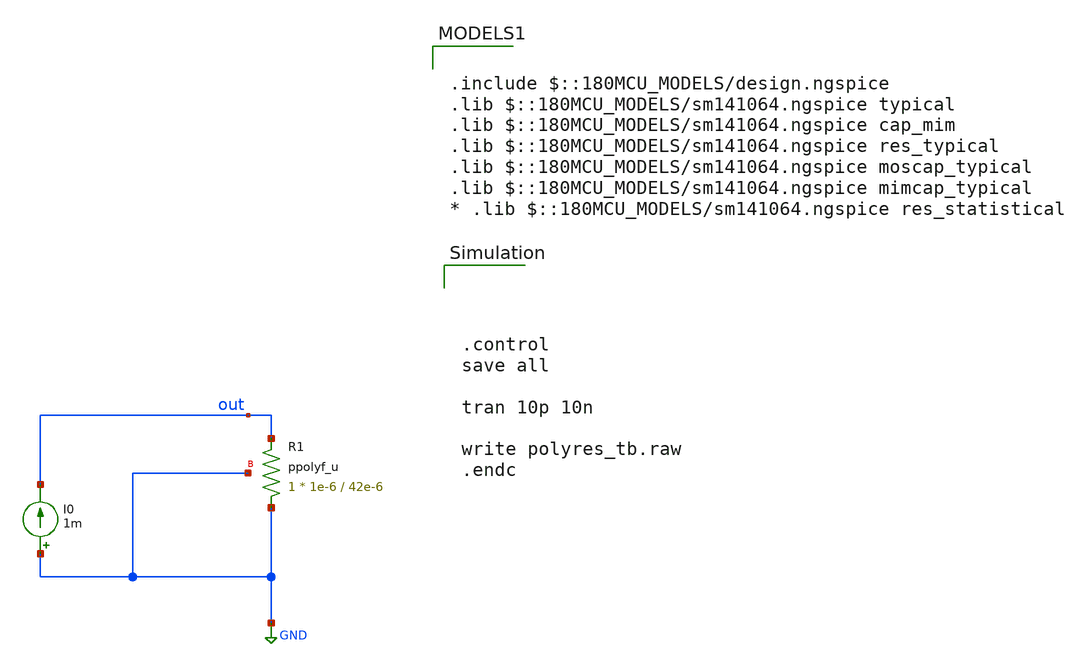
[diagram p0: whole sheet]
** sch_path: designs/libs/qw_core_analog/polyres_tb.sch
**.subckt polyres_tb
XR1 GND out GND ppolyf_u r_width=1e-6 r_length=42e-6 m=1
I0 GND out 1m
**** begin user architecture code




.control
save all

tran 10p 10n

write polyres_tb.raw
.endc




.include $::180MCU_MODELS/design.ngspice
.lib $::180MCU_MODELS/sm141064.ngspice typical
.lib $::180MCU_MODELS/sm141064.ngspice cap_mim
.lib $::180MCU_MODELS/sm141064.ngspice res_typical
.lib $::180MCU_MODELS/sm141064.ngspice moscap_typical
.lib $::180MCU_MODELS/sm141064.ngspice mimcap_typical
* .lib $::180MCU_MODELS/sm141064.ngspice res_statistical

**** end user architecture code
**.ends
.GLOBAL GND
.end
